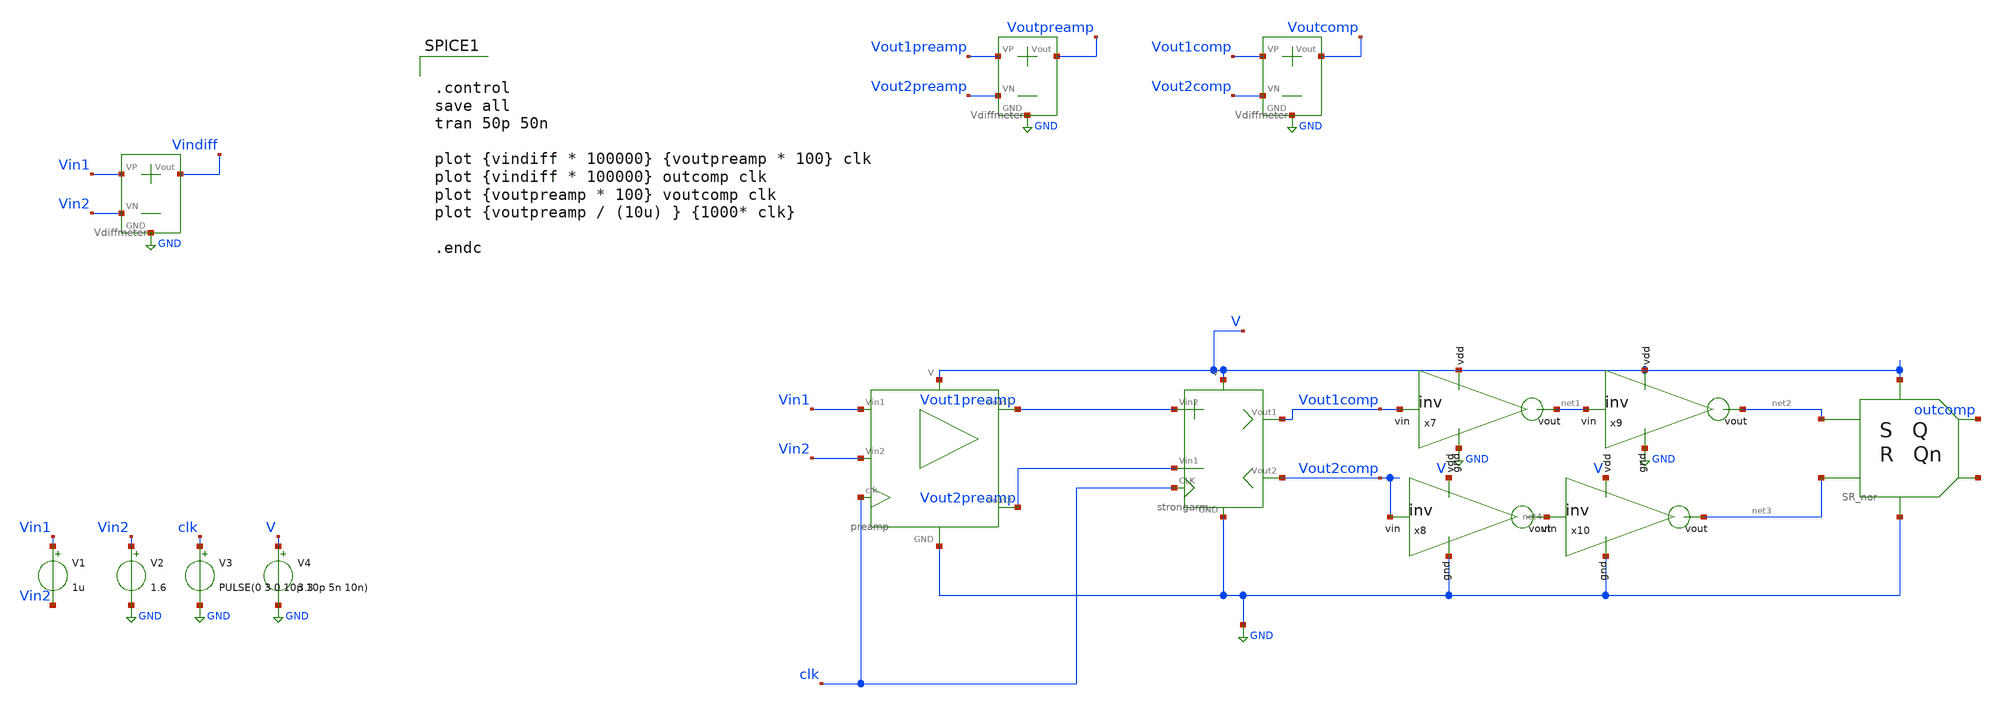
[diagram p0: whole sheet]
** sch_path: SAR_ADC/xschem/test/comp_full_tb/no_symbol/dc_10u__tb.sch
**.subckt dc_10u__tb
V1 Vin1 Vin2 1u
V2 Vin2 GND 1.6
V3 clk GND PULSE(0 3 0 10p 10p 5n 10n)
V4 V GND 3.3
X2 Vout1preamp Vout2preamp Voutpreamp GND Vdiffmeter
X6 Vout1comp Vout2comp Voutcomp GND Vdiffmeter
X5 Vin1 Vin2 Vindiff GND Vdiffmeter
x9 V GND net2 net1 inv cl=0.28u wp=0.44u wn=0.22u
x7 V GND net1 Vout1comp inv cl=0.28u wp=0.44u wn=0.22u
x8 V GND net4 Vout2comp inv cl=0.28u wp=0.44u wn=0.22u
x10 V GND net3 net4 inv cl=0.28u wp=0.44u wn=0.22u
X11 net2 V GND net3 outcomp net5 SR_nor
X1 V GND Vin1 clk Vout1preamp Vout2preamp Vin2 preamp
X12 V GND Vout2preamp Vout1preamp clk Vout1comp Vout2comp strongarm
**** begin user architecture code


.control
save all
tran 50p 50n

plot {vindiff * 100000} {voutpreamp * 100} clk
plot {vindiff * 100000} outcomp clk
plot {voutpreamp * 100} voutcomp clk
plot {voutpreamp / (10u) } {1000* clk}

.endc


.include $env(PDK_ROOT)/$env(PDK)/libs.tech/ngspice/design.ngspice
.lib $env(PDK_ROOT)/$env(PDK)/libs.tech/ngspice/sm141064.ngspice typical

**** end user architecture code
**.ends

* expanding   symbol:  ../../../../symbols/Vdiffmeter.sym # of pins=4
** sym_path: SAR_ADC/xschem/spice/symbols/Vdiffmeter.sym
** sch_path: SAR_ADC/xschem/spice/symbols/Vdiffmeter.sch
.subckt Vdiffmeter VP VN Vout GND
*.iopin Vout
*.iopin GND
*.iopin VP
*.iopin VN
R4 Vout GND 1k m=1
E4 Vout GND VP VN 1
.ends


* expanding   symbol:  ../../../../symbols/inv.sym # of pins=4
** sym_path: SAR_ADC/xschem/spice/inv.sym
** sch_path: SAR_ADC/xschem/spice/inv.sch
.subckt inv vdd gnd vout vin  cl=0.28u wp=0.44u wn=0.22u
*.ipin gnd
*.ipin vdd
*.ipin vin
*.opin vout
XM1 gnd vin vout gnd nfet_03v3 L=0.28u W=4u nf=1 ad='int((nf+1)/2) * W/nf * 0.18u' as='int((nf+2)/2) * W/nf * 0.18u'
+ pd='2*int((nf+1)/2) * (W/nf + 0.18u)' ps='2*int((nf+2)/2) * (W/nf + 0.18u)' nrd='0.18u / W' nrs='0.18u / W'
+ sa=0 sb=0 sd=0 m=1
XM2 vdd vin vout vdd pfet_03v3 L=0.28u W=4u nf=1 ad='int((nf+1)/2) * W/nf * 0.18u' as='int((nf+2)/2) * W/nf * 0.18u'
+ pd='2*int((nf+1)/2) * (W/nf + 0.18u)' ps='2*int((nf+2)/2) * (W/nf + 0.18u)' nrd='0.18u / W' nrs='0.18u / W'
+ sa=0 sb=0 sd=0 m=1
.ends


* expanding   symbol:  ../../../../symbols/SR_nor.sym # of pins=6
** sym_path: SAR_ADC/xschem/designs/SR_nor.sym
** sch_path: SAR_ADC/xschem/designs/SR_nor.sch
.subckt SR_nor S V GND R Q Qn
*.iopin V
*.iopin GND
*.iopin S
*.iopin R
*.iopin Qn
*.iopin Q
X1 S Q Qn GND V norgate
X2 Qn R Q GND V norgate
.ends


* expanding   symbol:  ../../../../symbols/preamp.sym # of pins=7
** sym_path: SAR_ADC/xschem/designs/preamp.sym
** sch_path: SAR_ADC/xschem/designs/preamp.sch
.subckt preamp V GND Vin1 clk Vout1 Vout2 Vin2
*.iopin V
*.iopin GND
*.iopin Vout2
*.iopin Vout1
*.iopin clk
*.iopin Vin2
*.iopin Vin1
XM26 Vout2 clk GND GND nfet_03v3 L=.5u W=.22u nf=1 ad='int((nf+1)/2) * W/nf * 0.18u' as='int((nf+2)/2) * W/nf * 0.18u'
+ pd='2*int((nf+1)/2) * (W/nf + 0.18u)' ps='2*int((nf+2)/2) * (W/nf + 0.18u)' nrd='0.18u / W' nrs='0.18u / W'
+ sa=0 sb=0 sd=0 m=1
XM27 Vout1 clk GND GND nfet_03v3 L=.5u W=.22u nf=1 ad='int((nf+1)/2) * W/nf * 0.18u' as='int((nf+2)/2) * W/nf * 0.18u'
+ pd='2*int((nf+1)/2) * (W/nf + 0.18u)' ps='2*int((nf+2)/2) * (W/nf + 0.18u)' nrd='0.18u / W' nrs='0.18u / W'
+ sa=0 sb=0 sd=0 m=1
XM24 Vout1 Vin2 net1 V pfet_03v3 L=.28u W=8u nf=1 ad='int((nf+1)/2) * W/nf * 0.18u' as='int((nf+2)/2) * W/nf * 0.18u'
+ pd='2*int((nf+1)/2) * (W/nf + 0.18u)' ps='2*int((nf+2)/2) * (W/nf + 0.18u)' nrd='0.18u / W' nrs='0.18u / W'
+ sa=0 sb=0 sd=0 m=1
XM25 Vout2 Vin1 net1 V pfet_03v3 L=.28u W=8u nf=1 ad='int((nf+1)/2) * W/nf * 0.18u' as='int((nf+2)/2) * W/nf * 0.18u'
+ pd='2*int((nf+1)/2) * (W/nf + 0.18u)' ps='2*int((nf+2)/2) * (W/nf + 0.18u)' nrd='0.18u / W' nrs='0.18u / W'
+ sa=0 sb=0 sd=0 m=1
XM1 V clk net1 V pfet_03v3 L=2u W=1u nf=1 ad='int((nf+1)/2) * W/nf * 0.18u' as='int((nf+2)/2) * W/nf * 0.18u'
+ pd='2*int((nf+1)/2) * (W/nf + 0.18u)' ps='2*int((nf+2)/2) * (W/nf + 0.18u)' nrd='0.18u / W' nrs='0.18u / W'
+ sa=0 sb=0 sd=0 m=1
.ends


* expanding   symbol:  ../../../../symbols/strongarm.sym # of pins=7
** sym_path: SAR_ADC/xschem/designs/strongarm.sym
** sch_path: SAR_ADC/xschem/designs/strongarm.sch
.subckt strongarm V GND Vin1 Vin2 CLK Vout1 Vout2
*.iopin V
*.iopin Vout1
*.iopin Vin1
*.iopin Vin2
*.iopin Vout2
*.iopin CLK
*.iopin GND
XM1 net3 Vout2 V V pfet_03v3 L=0.28u W=2u nf=1 ad='int((nf+1)/2) * W/nf * 0.18u' as='int((nf+2)/2) * W/nf * 0.18u'
+ pd='2*int((nf+1)/2) * (W/nf + 0.18u)' ps='2*int((nf+2)/2) * (W/nf + 0.18u)' nrd='0.18u / W' nrs='0.18u / W'
+ sa=0 sb=0 sd=0 m=1
XM2 Vout1 net1 GND GND nfet_03v3 L=0.28u W=2u nf=1 ad='int((nf+1)/2) * W/nf * 0.18u' as='int((nf+2)/2) * W/nf * 0.18u'
+ pd='2*int((nf+1)/2) * (W/nf + 0.18u)' ps='2*int((nf+2)/2) * (W/nf + 0.18u)' nrd='0.18u / W' nrs='0.18u / W'
+ sa=0 sb=0 sd=0 m=1
XM3 Vout2 Vout1 GND GND nfet_03v3 L=0.28u W=2u nf=1 ad='int((nf+1)/2) * W/nf * 0.18u' as='int((nf+2)/2) * W/nf * 0.18u'
+ pd='2*int((nf+1)/2) * (W/nf + 0.18u)' ps='2*int((nf+2)/2) * (W/nf + 0.18u)' nrd='0.18u / W' nrs='0.18u / W'
+ sa=0 sb=0 sd=0 m=1
XM4 Vout2 net1 GND GND nfet_03v3 L=0.28u W=2u nf=1 ad='int((nf+1)/2) * W/nf * 0.18u' as='int((nf+2)/2) * W/nf * 0.18u'
+ pd='2*int((nf+1)/2) * (W/nf + 0.18u)' ps='2*int((nf+2)/2) * (W/nf + 0.18u)' nrd='0.18u / W' nrs='0.18u / W'
+ sa=0 sb=0 sd=0 m=1
XM5 Vout1 Vout2 GND GND nfet_03v3 L=0.28u W=2u nf=1 ad='int((nf+1)/2) * W/nf * 0.18u' as='int((nf+2)/2) * W/nf * 0.18u'
+ pd='2*int((nf+1)/2) * (W/nf + 0.18u)' ps='2*int((nf+2)/2) * (W/nf + 0.18u)' nrd='0.18u / W' nrs='0.18u / W'
+ sa=0 sb=0 sd=0 m=1
XM6 net2 Vout1 V V pfet_03v3 L=0.28u W=2u nf=1 ad='int((nf+1)/2) * W/nf * 0.18u' as='int((nf+2)/2) * W/nf * 0.18u'
+ pd='2*int((nf+1)/2) * (W/nf + 0.18u)' ps='2*int((nf+2)/2) * (W/nf + 0.18u)' nrd='0.18u / W' nrs='0.18u / W'
+ sa=0 sb=0 sd=0 m=1
XM7 Vout1 Vin1 net3 V pfet_03v3 L=0.28u W=10u nf=1 ad='int((nf+1)/2) * W/nf * 0.18u' as='int((nf+2)/2) * W/nf * 0.18u'
+ pd='2*int((nf+1)/2) * (W/nf + 0.18u)' ps='2*int((nf+2)/2) * (W/nf + 0.18u)' nrd='0.18u / W' nrs='0.18u / W'
+ sa=0 sb=0 sd=0 m=1
XM8 Vout2 Vin2 net2 V pfet_03v3 L=0.28u W=10u nf=1 ad='int((nf+1)/2) * W/nf * 0.18u' as='int((nf+2)/2) * W/nf * 0.18u'
+ pd='2*int((nf+1)/2) * (W/nf + 0.18u)' ps='2*int((nf+2)/2) * (W/nf + 0.18u)' nrd='0.18u / W' nrs='0.18u / W'
+ sa=0 sb=0 sd=0 m=1
x1 V GND net4 CLK inv cl=0.28u wp=0.44u wn=0.22u wx=4u
x2 V GND net1 net4 inv cl=0.28u wp=0.44u wn=0.22u wx=4u
.ends


* expanding   symbol:  norgate.sym # of pins=5
** sym_path: SAR_ADC/xschem/designs/norgate.sym
** sch_path: SAR_ADC/xschem/designs/norgate.sch
.subckt norgate A B Z GND V
*.iopin GND
*.iopin A
*.iopin B
*.iopin V
*.iopin Z
XM3 V A net2 V pfet_03v3 L=0.28u W=0.22u nf=1 ad='int((nf+1)/2) * W/nf * 0.18u' as='int((nf+2)/2) * W/nf * 0.18u'
+ pd='2*int((nf+1)/2) * (W/nf + 0.18u)' ps='2*int((nf+2)/2) * (W/nf + 0.18u)' nrd='0.18u / W' nrs='0.18u / W'
+ sa=0 sb=0 sd=0 m=1
XM6 net2 B Z V pfet_03v3 L=0.28u W=0.22u nf=1 ad='int((nf+1)/2) * W/nf * 0.18u' as='int((nf+2)/2) * W/nf * 0.18u'
+ pd='2*int((nf+1)/2) * (W/nf + 0.18u)' ps='2*int((nf+2)/2) * (W/nf + 0.18u)' nrd='0.18u / W' nrs='0.18u / W'
+ sa=0 sb=0 sd=0 m=1
XM9 V B net1 V pfet_03v3 L=0.28u W=0.22u nf=1 ad='int((nf+1)/2) * W/nf * 0.18u' as='int((nf+2)/2) * W/nf * 0.18u'
+ pd='2*int((nf+1)/2) * (W/nf + 0.18u)' ps='2*int((nf+2)/2) * (W/nf + 0.18u)' nrd='0.18u / W' nrs='0.18u / W'
+ sa=0 sb=0 sd=0 m=1
XM12 net1 A Z V pfet_03v3 L=0.28u W=0.22u nf=1 ad='int((nf+1)/2) * W/nf * 0.18u' as='int((nf+2)/2) * W/nf * 0.18u'
+ pd='2*int((nf+1)/2) * (W/nf + 0.18u)' ps='2*int((nf+2)/2) * (W/nf + 0.18u)' nrd='0.18u / W' nrs='0.18u / W'
+ sa=0 sb=0 sd=0 m=1
XM2 Z B GND GND nfet_03v3 L=0.28u W=0.22u nf=1 ad='int((nf+1)/2) * W/nf * 0.18u' as='int((nf+2)/2) * W/nf * 0.18u'
+ pd='2*int((nf+1)/2) * (W/nf + 0.18u)' ps='2*int((nf+2)/2) * (W/nf + 0.18u)' nrd='0.18u / W' nrs='0.18u / W'
+ sa=0 sb=0 sd=0 m=1
XM4 Z A GND GND nfet_03v3 L=0.28u W=0.22u nf=1 ad='int((nf+1)/2) * W/nf * 0.18u' as='int((nf+2)/2) * W/nf * 0.18u'
+ pd='2*int((nf+1)/2) * (W/nf + 0.18u)' ps='2*int((nf+2)/2) * (W/nf + 0.18u)' nrd='0.18u / W' nrs='0.18u / W'
+ sa=0 sb=0 sd=0 m=1
.ends

.GLOBAL GND
.end
